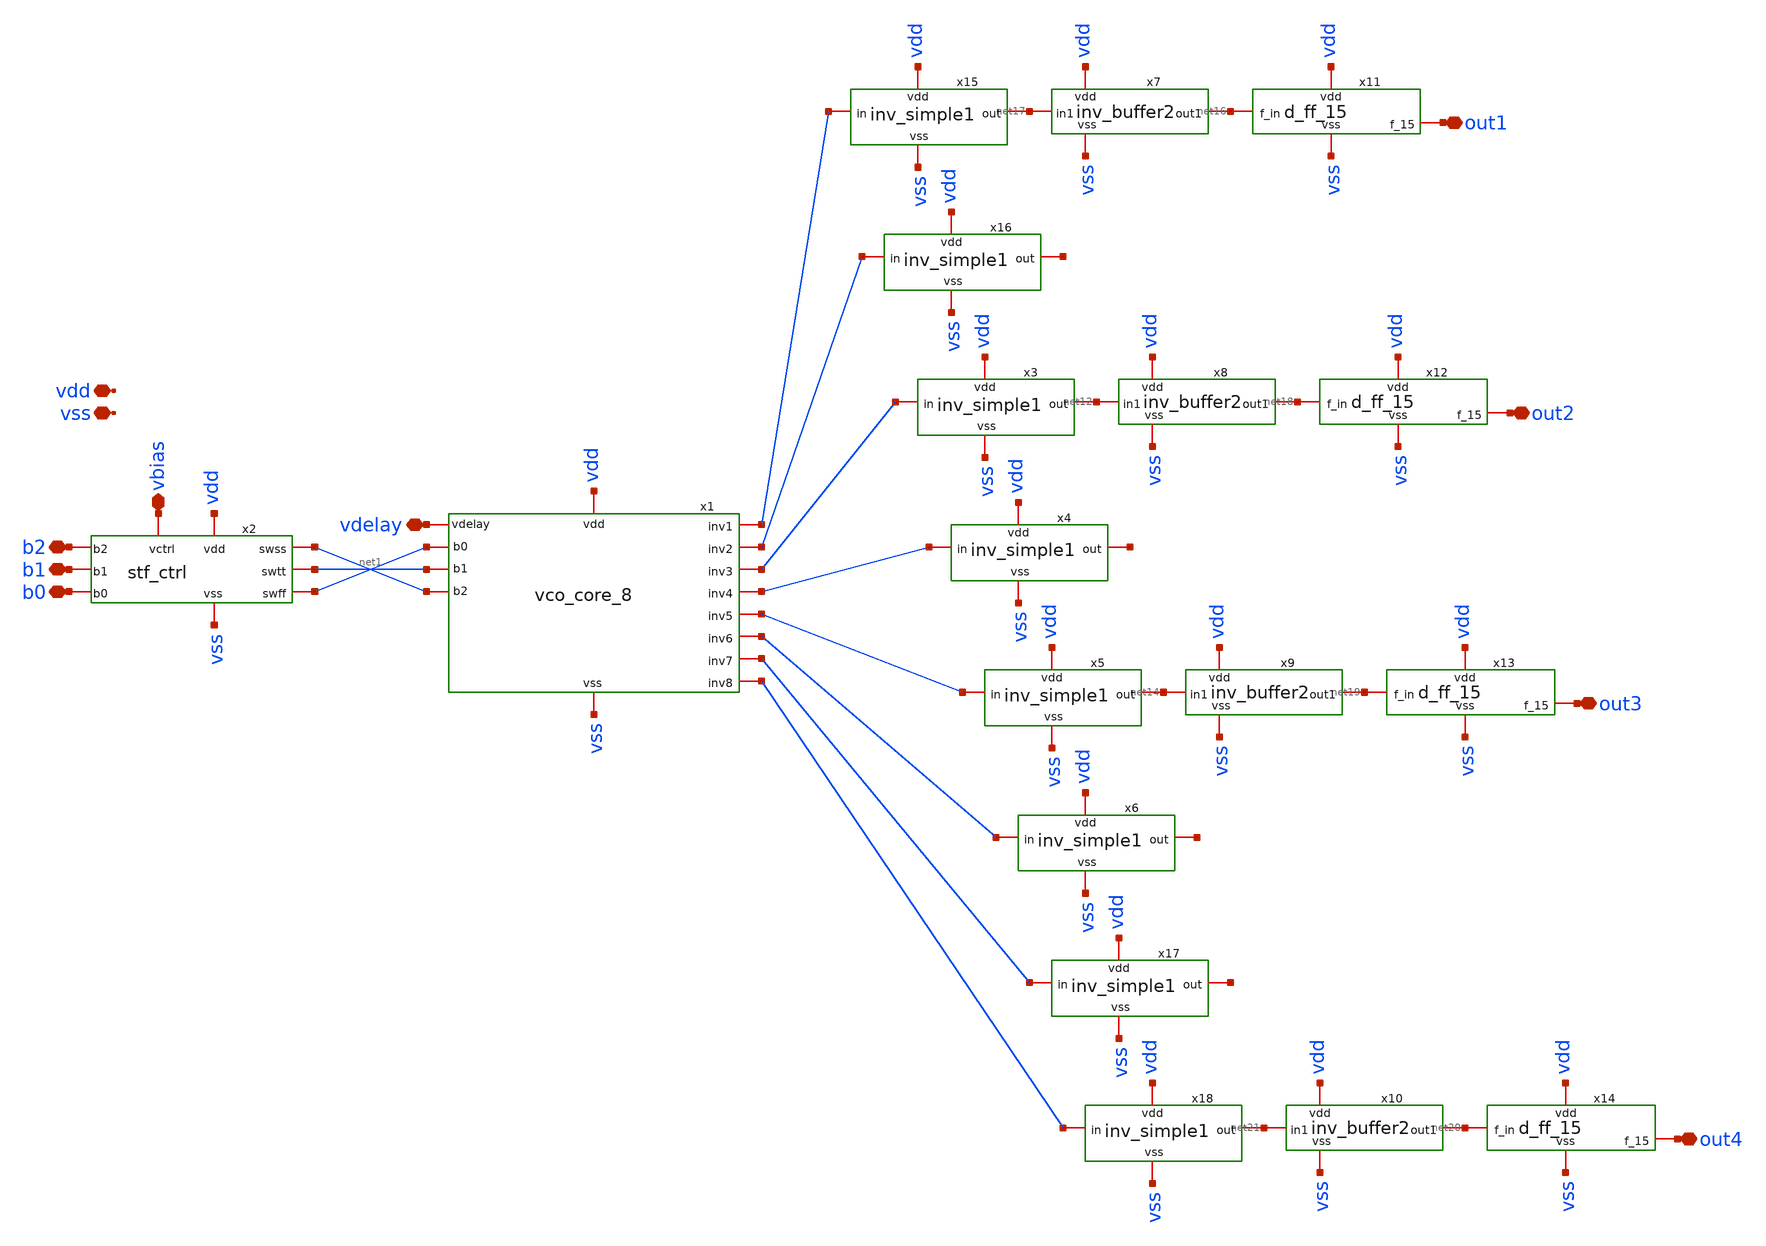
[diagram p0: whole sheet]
** sch_path: xschem/full_vco_1.sch
**.subckt full_vco_1 vdd vss vdelay b0 b1 b2 out1 out2 out3 out4 vbias
*.iopin vdd
*.iopin vss
*.iopin vdelay
*.iopin b0
*.iopin b1
*.iopin b2
*.iopin out1
*.iopin out2
*.iopin out3
*.iopin out4
*.iopin vbias
x1 net4 vdd vss net5 net6 vdelay net7 net8 net3 net1 net9 net10 net2 net11 vco_core_8
x2 vbias vdd b2 net2 b1 net1 net3 b0 vss stf_ctrl
x3 vdd net6 net12 vss inv_simple1
x4 vdd net7 net13 vss inv_simple1
x5 vdd net8 net14 vss inv_simple1
x6 vdd net9 net15 vss inv_simple1
x7 vdd vss net16 net17 inv_buffer2
x8 vdd vss net18 net12 inv_buffer2
x9 vdd vss net19 net14 inv_buffer2
x10 vdd vss net20 net21 inv_buffer2
x11 vdd vss net16 out1 d_ff_15
x12 vdd vss net18 out2 d_ff_15
x13 vdd vss net19 out3 d_ff_15
x14 vdd vss net20 out4 d_ff_15
x15 vdd net4 net17 vss inv_simple1
x16 vdd net5 net22 vss inv_simple1
x17 vdd net10 net23 vss inv_simple1
x18 vdd net11 net21 vss inv_simple1
**.ends
.end
